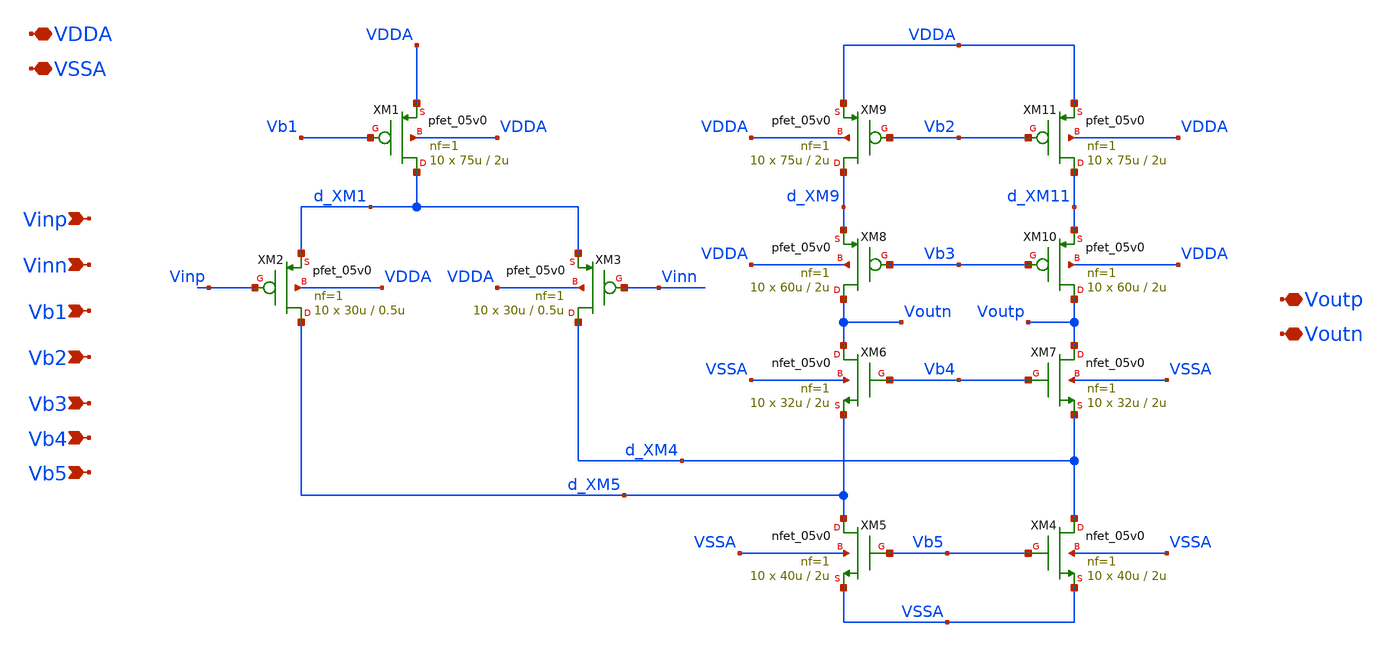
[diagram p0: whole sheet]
** sch_path: schematic/folded_cascode_bk.sch
**.subckt folded_cascode_bk Vinp Vinn VDDA VSSA Vb1 Vb2 Vb3 Vb4 Vb5 Voutp Voutn
*.ipin Vinp
*.ipin Vinn
*.iopin VDDA
*.iopin VSSA
*.ipin Vb1
*.ipin Vb2
*.ipin Vb3
*.ipin Vb4
*.ipin Vb5
*.iopin Voutp
*.iopin Voutn
XM1 d_XM1 Vb1 VDDA VDDA pfet_05v0 L=2u W=75u nf=1 ad='int((nf+1)/2) * W/nf * 0.18u' as='int((nf+2)/2) * W/nf * 0.18u'
+ pd='2*int((nf+1)/2) * (W/nf + 0.18u)' ps='2*int((nf+2)/2) * (W/nf + 0.18u)' nrd='0.18u / W' nrs='0.18u / W'
+ sa=0 sb=0 sd=0 m=10
XM2 d_XM5 Vinp d_XM1 VDDA pfet_05v0 L=0.5u W=30u nf=1 ad='int((nf+1)/2) * W/nf * 0.18u' as='int((nf+2)/2) * W/nf * 0.18u'
+ pd='2*int((nf+1)/2) * (W/nf + 0.18u)' ps='2*int((nf+2)/2) * (W/nf + 0.18u)' nrd='0.18u / W' nrs='0.18u / W'
+ sa=0 sb=0 sd=0 m=10
XM3 d_XM4 Vinn d_XM1 VDDA pfet_05v0 L=0.5u W=30u nf=1 ad='int((nf+1)/2) * W/nf * 0.18u' as='int((nf+2)/2) * W/nf * 0.18u'
+ pd='2*int((nf+1)/2) * (W/nf + 0.18u)' ps='2*int((nf+2)/2) * (W/nf + 0.18u)' nrd='0.18u / W' nrs='0.18u / W'
+ sa=0 sb=0 sd=0 m=10
XM4 d_XM4 Vb5 VSSA VSSA nfet_05v0 L=2u W=40u nf=1 ad='int((nf+1)/2) * W/nf * 0.18u' as='int((nf+2)/2) * W/nf * 0.18u'
+ pd='2*int((nf+1)/2) * (W/nf + 0.18u)' ps='2*int((nf+2)/2) * (W/nf + 0.18u)' nrd='0.18u / W' nrs='0.18u / W'
+ sa=0 sb=0 sd=0 m=10
XM5 d_XM5 Vb5 VSSA VSSA nfet_05v0 L=2u W=40u nf=1 ad='int((nf+1)/2) * W/nf * 0.18u' as='int((nf+2)/2) * W/nf * 0.18u'
+ pd='2*int((nf+1)/2) * (W/nf + 0.18u)' ps='2*int((nf+2)/2) * (W/nf + 0.18u)' nrd='0.18u / W' nrs='0.18u / W'
+ sa=0 sb=0 sd=0 m=10
XM6 Voutn Vb4 d_XM5 VSSA nfet_05v0 L=2u W=32u nf=1 ad='int((nf+1)/2) * W/nf * 0.18u' as='int((nf+2)/2) * W/nf * 0.18u'
+ pd='2*int((nf+1)/2) * (W/nf + 0.18u)' ps='2*int((nf+2)/2) * (W/nf + 0.18u)' nrd='0.18u / W' nrs='0.18u / W'
+ sa=0 sb=0 sd=0 m=10
XM7 Voutp Vb4 d_XM4 VSSA nfet_05v0 L=2u W=32u nf=1 ad='int((nf+1)/2) * W/nf * 0.18u' as='int((nf+2)/2) * W/nf * 0.18u'
+ pd='2*int((nf+1)/2) * (W/nf + 0.18u)' ps='2*int((nf+2)/2) * (W/nf + 0.18u)' nrd='0.18u / W' nrs='0.18u / W'
+ sa=0 sb=0 sd=0 m=10
XM8 Voutn Vb3 d_XM9 VDDA pfet_05v0 L=2u W=60u nf=1 ad='int((nf+1)/2) * W/nf * 0.18u' as='int((nf+2)/2) * W/nf * 0.18u'
+ pd='2*int((nf+1)/2) * (W/nf + 0.18u)' ps='2*int((nf+2)/2) * (W/nf + 0.18u)' nrd='0.18u / W' nrs='0.18u / W'
+ sa=0 sb=0 sd=0 m=10
XM9 d_XM9 Vb2 VDDA VDDA pfet_05v0 L=2u W=75u nf=1 ad='int((nf+1)/2) * W/nf * 0.18u' as='int((nf+2)/2) * W/nf * 0.18u'
+ pd='2*int((nf+1)/2) * (W/nf + 0.18u)' ps='2*int((nf+2)/2) * (W/nf + 0.18u)' nrd='0.18u / W' nrs='0.18u / W'
+ sa=0 sb=0 sd=0 m=10
XM10 Voutp Vb3 d_XM11 VDDA pfet_05v0 L=2u W=60u nf=1 ad='int((nf+1)/2) * W/nf * 0.18u' as='int((nf+2)/2) * W/nf * 0.18u'
+ pd='2*int((nf+1)/2) * (W/nf + 0.18u)' ps='2*int((nf+2)/2) * (W/nf + 0.18u)' nrd='0.18u / W' nrs='0.18u / W'
+ sa=0 sb=0 sd=0 m=10
XM11 d_XM11 Vb2 VDDA VDDA pfet_05v0 L=2u W=75u nf=1 ad='int((nf+1)/2) * W/nf * 0.18u' as='int((nf+2)/2) * W/nf * 0.18u'
+ pd='2*int((nf+1)/2) * (W/nf + 0.18u)' ps='2*int((nf+2)/2) * (W/nf + 0.18u)' nrd='0.18u / W' nrs='0.18u / W'
+ sa=0 sb=0 sd=0 m=10
**.ends
.end
